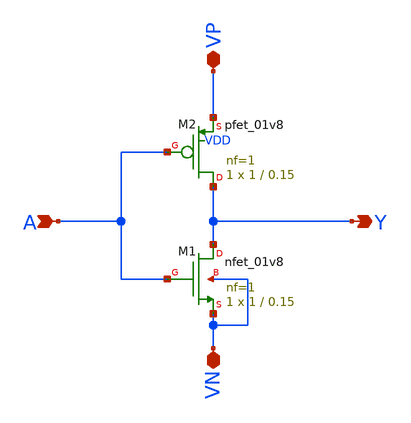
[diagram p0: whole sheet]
** sch_path: xschem/schemetic_symbol/inverter_tutorial/inverter.sch
**.subckt inverter A VP VN Y
*.ipin A
*.iopin VP
*.iopin VN
*.opin Y
XM1 Y A VN VN sky130_fd_pr__nfet_01v8 L=0.15 W=1 nf=1 ad='int((nf+1)/2) * W/nf * 0.29' as='int((nf+2)/2) * W/nf * 0.29'
+ pd='2*int((nf+1)/2) * (W/nf + 0.29)' ps='2*int((nf+2)/2) * (W/nf + 0.29)' nrd='0.29 / W' nrs='0.29 / W'
+ sa=0 sb=0 sd=0 mult=1 m=1
XM2 Y A VP VDD sky130_fd_pr__pfet_01v8 L=0.15 W=1 nf=1 ad='int((nf+1)/2) * W/nf * 0.29' as='int((nf+2)/2) * W/nf * 0.29'
+ pd='2*int((nf+1)/2) * (W/nf + 0.29)' ps='2*int((nf+2)/2) * (W/nf + 0.29)' nrd='0.29 / W' nrs='0.29 / W'
+ sa=0 sb=0 sd=0 mult=1 m=1
**.ends
.end
